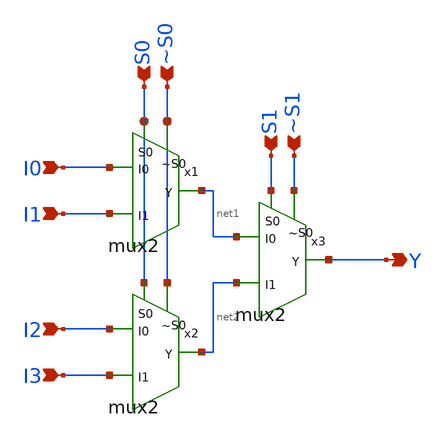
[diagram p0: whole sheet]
** sch_path: circuits/xschem/mux4.sch
**.subckt mux4 I0 I1 I2 I3 S0 ~S0 S1 ~S1 Y
*.ipin I0
*.ipin I1
*.ipin I2
*.ipin I3
*.ipin S0
*.ipin ~S0
*.ipin S1
*.ipin ~S1
*.opin Y
x1 I1 I0 S0 net1 ~S0 mux2
x2 I3 I2 S0 net2 ~S0 mux2
x3 net2 net1 S1 Y ~S1 mux2
**.ends
.end
